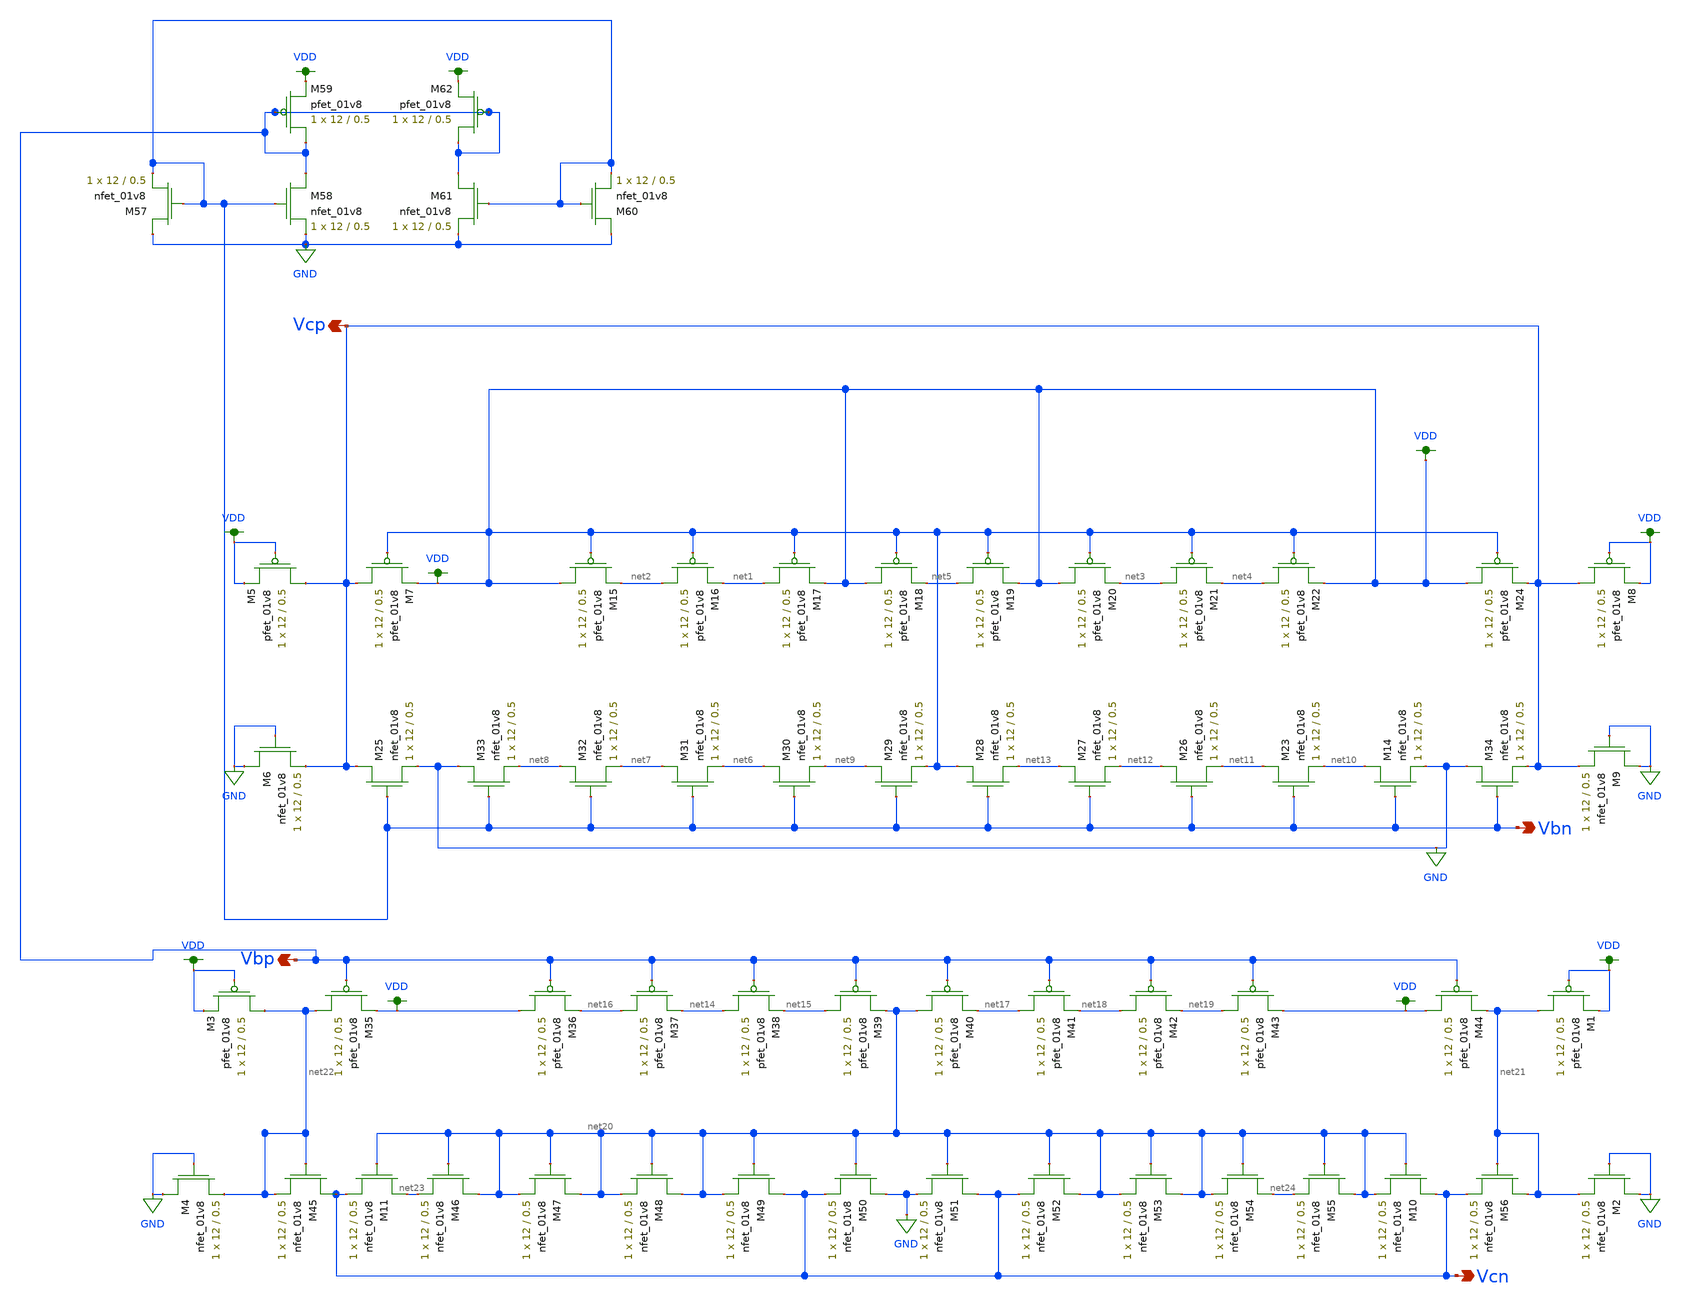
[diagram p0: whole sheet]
** sch_path: miniproject3/LVS_BIASGEN.sch
**.subckt LVS_BIASGEN Vbp Vcn Vcp Vbn
*.opin Vbp
*.opin Vcn
*.opin Vcp
*.opin Vbn
XM7 Vcp VDD VDD VDD sky130_fd_pr__pfet_01v8 L=0.5 W=12 nf=1 ad='int((nf+1)/2) * W/nf * 0.29' as='int((nf+2)/2) * W/nf * 0.29'
+ pd='2*int((nf+1)/2) * (W/nf + 0.29)' ps='2*int((nf+2)/2) * (W/nf + 0.29)' nrd='0.29 / W' nrs='0.29 / W'
+ sa=0 sb=0 sd=0 mult=1 m=1
XM15 VDD VDD net2 VDD sky130_fd_pr__pfet_01v8 L=0.5 W=12 nf=1 ad='int((nf+1)/2) * W/nf * 0.29' as='int((nf+2)/2) * W/nf * 0.29'
+ pd='2*int((nf+1)/2) * (W/nf + 0.29)' ps='2*int((nf+2)/2) * (W/nf + 0.29)' nrd='0.29 / W' nrs='0.29 / W'
+ sa=0 sb=0 sd=0 mult=1 m=1
XM16 net2 VDD net1 VDD sky130_fd_pr__pfet_01v8 L=0.5 W=12 nf=1 ad='int((nf+1)/2) * W/nf * 0.29' as='int((nf+2)/2) * W/nf * 0.29'
+ pd='2*int((nf+1)/2) * (W/nf + 0.29)' ps='2*int((nf+2)/2) * (W/nf + 0.29)' nrd='0.29 / W' nrs='0.29 / W'
+ sa=0 sb=0 sd=0 mult=1 m=1
XM17 net1 VDD VDD VDD sky130_fd_pr__pfet_01v8 L=0.5 W=12 nf=1 ad='int((nf+1)/2) * W/nf * 0.29' as='int((nf+2)/2) * W/nf * 0.29'
+ pd='2*int((nf+1)/2) * (W/nf + 0.29)' ps='2*int((nf+2)/2) * (W/nf + 0.29)' nrd='0.29 / W' nrs='0.29 / W'
+ sa=0 sb=0 sd=0 mult=1 m=1
XM18 VDD VDD net5 VDD sky130_fd_pr__pfet_01v8 L=0.5 W=12 nf=1 ad='int((nf+1)/2) * W/nf * 0.29' as='int((nf+2)/2) * W/nf * 0.29'
+ pd='2*int((nf+1)/2) * (W/nf + 0.29)' ps='2*int((nf+2)/2) * (W/nf + 0.29)' nrd='0.29 / W' nrs='0.29 / W'
+ sa=0 sb=0 sd=0 mult=1 m=1
XM19 net5 VDD VDD VDD sky130_fd_pr__pfet_01v8 L=0.5 W=12 nf=1 ad='int((nf+1)/2) * W/nf * 0.29' as='int((nf+2)/2) * W/nf * 0.29'
+ pd='2*int((nf+1)/2) * (W/nf + 0.29)' ps='2*int((nf+2)/2) * (W/nf + 0.29)' nrd='0.29 / W' nrs='0.29 / W'
+ sa=0 sb=0 sd=0 mult=1 m=1
XM20 VDD VDD net3 VDD sky130_fd_pr__pfet_01v8 L=0.5 W=12 nf=1 ad='int((nf+1)/2) * W/nf * 0.29' as='int((nf+2)/2) * W/nf * 0.29'
+ pd='2*int((nf+1)/2) * (W/nf + 0.29)' ps='2*int((nf+2)/2) * (W/nf + 0.29)' nrd='0.29 / W' nrs='0.29 / W'
+ sa=0 sb=0 sd=0 mult=1 m=1
XM21 net3 VDD net4 VDD sky130_fd_pr__pfet_01v8 L=0.5 W=12 nf=1 ad='int((nf+1)/2) * W/nf * 0.29' as='int((nf+2)/2) * W/nf * 0.29'
+ pd='2*int((nf+1)/2) * (W/nf + 0.29)' ps='2*int((nf+2)/2) * (W/nf + 0.29)' nrd='0.29 / W' nrs='0.29 / W'
+ sa=0 sb=0 sd=0 mult=1 m=1
XM22 net4 VDD VDD VDD sky130_fd_pr__pfet_01v8 L=0.5 W=12 nf=1 ad='int((nf+1)/2) * W/nf * 0.29' as='int((nf+2)/2) * W/nf * 0.29'
+ pd='2*int((nf+1)/2) * (W/nf + 0.29)' ps='2*int((nf+2)/2) * (W/nf + 0.29)' nrd='0.29 / W' nrs='0.29 / W'
+ sa=0 sb=0 sd=0 mult=1 m=1
XM24 VDD VDD Vcp VDD sky130_fd_pr__pfet_01v8 L=0.5 W=12 nf=1 ad='int((nf+1)/2) * W/nf * 0.29' as='int((nf+2)/2) * W/nf * 0.29'
+ pd='2*int((nf+1)/2) * (W/nf + 0.29)' ps='2*int((nf+2)/2) * (W/nf + 0.29)' nrd='0.29 / W' nrs='0.29 / W'
+ sa=0 sb=0 sd=0 mult=1 m=1
XM25 Vcp Vbn GND GND sky130_fd_pr__nfet_01v8 L=0.5 W=12 nf=1 ad='int((nf+1)/2) * W/nf * 0.29' as='int((nf+2)/2) * W/nf * 0.29'
+ pd='2*int((nf+1)/2) * (W/nf + 0.29)' ps='2*int((nf+2)/2) * (W/nf + 0.29)' nrd='0.29 / W' nrs='0.29 / W'
+ sa=0 sb=0 sd=0 mult=1 m=1
XM14 net10 Vbn GND GND sky130_fd_pr__nfet_01v8 L=0.5 W=12 nf=1 ad='int((nf+1)/2) * W/nf * 0.29' as='int((nf+2)/2) * W/nf * 0.29'
+ pd='2*int((nf+1)/2) * (W/nf + 0.29)' ps='2*int((nf+2)/2) * (W/nf + 0.29)' nrd='0.29 / W' nrs='0.29 / W'
+ sa=0 sb=0 sd=0 mult=1 m=1
XM23 net11 Vbn net10 GND sky130_fd_pr__nfet_01v8 L=0.5 W=12 nf=1 ad='int((nf+1)/2) * W/nf * 0.29' as='int((nf+2)/2) * W/nf * 0.29'
+ pd='2*int((nf+1)/2) * (W/nf + 0.29)' ps='2*int((nf+2)/2) * (W/nf + 0.29)' nrd='0.29 / W' nrs='0.29 / W'
+ sa=0 sb=0 sd=0 mult=1 m=1
XM26 net12 Vbn net11 GND sky130_fd_pr__nfet_01v8 L=0.5 W=12 nf=1 ad='int((nf+1)/2) * W/nf * 0.29' as='int((nf+2)/2) * W/nf * 0.29'
+ pd='2*int((nf+1)/2) * (W/nf + 0.29)' ps='2*int((nf+2)/2) * (W/nf + 0.29)' nrd='0.29 / W' nrs='0.29 / W'
+ sa=0 sb=0 sd=0 mult=1 m=1
XM27 net13 Vbn net12 GND sky130_fd_pr__nfet_01v8 L=0.5 W=12 nf=1 ad='int((nf+1)/2) * W/nf * 0.29' as='int((nf+2)/2) * W/nf * 0.29'
+ pd='2*int((nf+1)/2) * (W/nf + 0.29)' ps='2*int((nf+2)/2) * (W/nf + 0.29)' nrd='0.29 / W' nrs='0.29 / W'
+ sa=0 sb=0 sd=0 mult=1 m=1
XM28 VDD Vbn net13 GND sky130_fd_pr__nfet_01v8 L=0.5 W=12 nf=1 ad='int((nf+1)/2) * W/nf * 0.29' as='int((nf+2)/2) * W/nf * 0.29'
+ pd='2*int((nf+1)/2) * (W/nf + 0.29)' ps='2*int((nf+2)/2) * (W/nf + 0.29)' nrd='0.29 / W' nrs='0.29 / W'
+ sa=0 sb=0 sd=0 mult=1 m=1
XM29 net9 Vbn VDD GND sky130_fd_pr__nfet_01v8 L=0.5 W=12 nf=1 ad='int((nf+1)/2) * W/nf * 0.29' as='int((nf+2)/2) * W/nf * 0.29'
+ pd='2*int((nf+1)/2) * (W/nf + 0.29)' ps='2*int((nf+2)/2) * (W/nf + 0.29)' nrd='0.29 / W' nrs='0.29 / W'
+ sa=0 sb=0 sd=0 mult=1 m=1
XM30 net6 Vbn net9 GND sky130_fd_pr__nfet_01v8 L=0.5 W=12 nf=1 ad='int((nf+1)/2) * W/nf * 0.29' as='int((nf+2)/2) * W/nf * 0.29'
+ pd='2*int((nf+1)/2) * (W/nf + 0.29)' ps='2*int((nf+2)/2) * (W/nf + 0.29)' nrd='0.29 / W' nrs='0.29 / W'
+ sa=0 sb=0 sd=0 mult=1 m=1
XM31 net7 Vbn net6 GND sky130_fd_pr__nfet_01v8 L=0.5 W=12 nf=1 ad='int((nf+1)/2) * W/nf * 0.29' as='int((nf+2)/2) * W/nf * 0.29'
+ pd='2*int((nf+1)/2) * (W/nf + 0.29)' ps='2*int((nf+2)/2) * (W/nf + 0.29)' nrd='0.29 / W' nrs='0.29 / W'
+ sa=0 sb=0 sd=0 mult=1 m=1
XM32 net8 Vbn net7 GND sky130_fd_pr__nfet_01v8 L=0.5 W=12 nf=1 ad='int((nf+1)/2) * W/nf * 0.29' as='int((nf+2)/2) * W/nf * 0.29'
+ pd='2*int((nf+1)/2) * (W/nf + 0.29)' ps='2*int((nf+2)/2) * (W/nf + 0.29)' nrd='0.29 / W' nrs='0.29 / W'
+ sa=0 sb=0 sd=0 mult=1 m=1
XM33 GND Vbn net8 GND sky130_fd_pr__nfet_01v8 L=0.5 W=12 nf=1 ad='int((nf+1)/2) * W/nf * 0.29' as='int((nf+2)/2) * W/nf * 0.29'
+ pd='2*int((nf+1)/2) * (W/nf + 0.29)' ps='2*int((nf+2)/2) * (W/nf + 0.29)' nrd='0.29 / W' nrs='0.29 / W'
+ sa=0 sb=0 sd=0 mult=1 m=1
XM34 GND Vbn Vcp GND sky130_fd_pr__nfet_01v8 L=0.5 W=12 nf=1 ad='int((nf+1)/2) * W/nf * 0.29' as='int((nf+2)/2) * W/nf * 0.29'
+ pd='2*int((nf+1)/2) * (W/nf + 0.29)' ps='2*int((nf+2)/2) * (W/nf + 0.29)' nrd='0.29 / W' nrs='0.29 / W'
+ sa=0 sb=0 sd=0 mult=1 m=1
XM35 net22 Vbp VDD VDD sky130_fd_pr__pfet_01v8 L=0.5 W=12 nf=1 ad='int((nf+1)/2) * W/nf * 0.29' as='int((nf+2)/2) * W/nf * 0.29'
+ pd='2*int((nf+1)/2) * (W/nf + 0.29)' ps='2*int((nf+2)/2) * (W/nf + 0.29)' nrd='0.29 / W' nrs='0.29 / W'
+ sa=0 sb=0 sd=0 mult=1 m=1
XM36 VDD Vbp net16 VDD sky130_fd_pr__pfet_01v8 L=0.5 W=12 nf=1 ad='int((nf+1)/2) * W/nf * 0.29' as='int((nf+2)/2) * W/nf * 0.29'
+ pd='2*int((nf+1)/2) * (W/nf + 0.29)' ps='2*int((nf+2)/2) * (W/nf + 0.29)' nrd='0.29 / W' nrs='0.29 / W'
+ sa=0 sb=0 sd=0 mult=1 m=1
XM37 net16 Vbp net14 VDD sky130_fd_pr__pfet_01v8 L=0.5 W=12 nf=1 ad='int((nf+1)/2) * W/nf * 0.29' as='int((nf+2)/2) * W/nf * 0.29'
+ pd='2*int((nf+1)/2) * (W/nf + 0.29)' ps='2*int((nf+2)/2) * (W/nf + 0.29)' nrd='0.29 / W' nrs='0.29 / W'
+ sa=0 sb=0 sd=0 mult=1 m=1
XM38 net14 Vbp net15 VDD sky130_fd_pr__pfet_01v8 L=0.5 W=12 nf=1 ad='int((nf+1)/2) * W/nf * 0.29' as='int((nf+2)/2) * W/nf * 0.29'
+ pd='2*int((nf+1)/2) * (W/nf + 0.29)' ps='2*int((nf+2)/2) * (W/nf + 0.29)' nrd='0.29 / W' nrs='0.29 / W'
+ sa=0 sb=0 sd=0 mult=1 m=1
XM39 net15 Vbp net20 VDD sky130_fd_pr__pfet_01v8 L=0.5 W=12 nf=1 ad='int((nf+1)/2) * W/nf * 0.29' as='int((nf+2)/2) * W/nf * 0.29'
+ pd='2*int((nf+1)/2) * (W/nf + 0.29)' ps='2*int((nf+2)/2) * (W/nf + 0.29)' nrd='0.29 / W' nrs='0.29 / W'
+ sa=0 sb=0 sd=0 mult=1 m=1
XM40 net20 Vbp net17 VDD sky130_fd_pr__pfet_01v8 L=0.5 W=12 nf=1 ad='int((nf+1)/2) * W/nf * 0.29' as='int((nf+2)/2) * W/nf * 0.29'
+ pd='2*int((nf+1)/2) * (W/nf + 0.29)' ps='2*int((nf+2)/2) * (W/nf + 0.29)' nrd='0.29 / W' nrs='0.29 / W'
+ sa=0 sb=0 sd=0 mult=1 m=1
XM41 net17 Vbp net18 VDD sky130_fd_pr__pfet_01v8 L=0.5 W=12 nf=1 ad='int((nf+1)/2) * W/nf * 0.29' as='int((nf+2)/2) * W/nf * 0.29'
+ pd='2*int((nf+1)/2) * (W/nf + 0.29)' ps='2*int((nf+2)/2) * (W/nf + 0.29)' nrd='0.29 / W' nrs='0.29 / W'
+ sa=0 sb=0 sd=0 mult=1 m=1
XM42 net18 Vbp net19 VDD sky130_fd_pr__pfet_01v8 L=0.5 W=12 nf=1 ad='int((nf+1)/2) * W/nf * 0.29' as='int((nf+2)/2) * W/nf * 0.29'
+ pd='2*int((nf+1)/2) * (W/nf + 0.29)' ps='2*int((nf+2)/2) * (W/nf + 0.29)' nrd='0.29 / W' nrs='0.29 / W'
+ sa=0 sb=0 sd=0 mult=1 m=1
XM43 net19 Vbp VDD VDD sky130_fd_pr__pfet_01v8 L=0.5 W=12 nf=1 ad='int((nf+1)/2) * W/nf * 0.29' as='int((nf+2)/2) * W/nf * 0.29'
+ pd='2*int((nf+1)/2) * (W/nf + 0.29)' ps='2*int((nf+2)/2) * (W/nf + 0.29)' nrd='0.29 / W' nrs='0.29 / W'
+ sa=0 sb=0 sd=0 mult=1 m=1
XM44 VDD Vbp net21 VDD sky130_fd_pr__pfet_01v8 L=0.5 W=12 nf=1 ad='int((nf+1)/2) * W/nf * 0.29' as='int((nf+2)/2) * W/nf * 0.29'
+ pd='2*int((nf+1)/2) * (W/nf + 0.29)' ps='2*int((nf+2)/2) * (W/nf + 0.29)' nrd='0.29 / W' nrs='0.29 / W'
+ sa=0 sb=0 sd=0 mult=1 m=1
XM45 Vcn net22 net22 GND sky130_fd_pr__nfet_01v8 L=0.5 W=12 nf=1 ad='int((nf+1)/2) * W/nf * 0.29' as='int((nf+2)/2) * W/nf * 0.29'
+ pd='2*int((nf+1)/2) * (W/nf + 0.29)' ps='2*int((nf+2)/2) * (W/nf + 0.29)' nrd='0.29 / W' nrs='0.29 / W'
+ sa=0 sb=0 sd=0 mult=1 m=1
XM46 net20 net20 net23 GND sky130_fd_pr__nfet_01v8 L=0.5 W=12 nf=1 ad='int((nf+1)/2) * W/nf * 0.29' as='int((nf+2)/2) * W/nf * 0.29'
+ pd='2*int((nf+1)/2) * (W/nf + 0.29)' ps='2*int((nf+2)/2) * (W/nf + 0.29)' nrd='0.29 / W' nrs='0.29 / W'
+ sa=0 sb=0 sd=0 mult=1 m=1
XM47 net20 net20 net20 GND sky130_fd_pr__nfet_01v8 L=0.5 W=12 nf=1 ad='int((nf+1)/2) * W/nf * 0.29' as='int((nf+2)/2) * W/nf * 0.29'
+ pd='2*int((nf+1)/2) * (W/nf + 0.29)' ps='2*int((nf+2)/2) * (W/nf + 0.29)' nrd='0.29 / W' nrs='0.29 / W'
+ sa=0 sb=0 sd=0 mult=1 m=1
XM48 net20 net20 net20 GND sky130_fd_pr__nfet_01v8 L=0.5 W=12 nf=1 ad='int((nf+1)/2) * W/nf * 0.29' as='int((nf+2)/2) * W/nf * 0.29'
+ pd='2*int((nf+1)/2) * (W/nf + 0.29)' ps='2*int((nf+2)/2) * (W/nf + 0.29)' nrd='0.29 / W' nrs='0.29 / W'
+ sa=0 sb=0 sd=0 mult=1 m=1
XM49 Vcn net20 net20 GND sky130_fd_pr__nfet_01v8 L=0.5 W=12 nf=1 ad='int((nf+1)/2) * W/nf * 0.29' as='int((nf+2)/2) * W/nf * 0.29'
+ pd='2*int((nf+1)/2) * (W/nf + 0.29)' ps='2*int((nf+2)/2) * (W/nf + 0.29)' nrd='0.29 / W' nrs='0.29 / W'
+ sa=0 sb=0 sd=0 mult=1 m=1
XM50 GND net20 Vcn GND sky130_fd_pr__nfet_01v8 L=0.5 W=12 nf=1 ad='int((nf+1)/2) * W/nf * 0.29' as='int((nf+2)/2) * W/nf * 0.29'
+ pd='2*int((nf+1)/2) * (W/nf + 0.29)' ps='2*int((nf+2)/2) * (W/nf + 0.29)' nrd='0.29 / W' nrs='0.29 / W'
+ sa=0 sb=0 sd=0 mult=1 m=1
XM51 Vcn net20 GND GND sky130_fd_pr__nfet_01v8 L=0.5 W=12 nf=1 ad='int((nf+1)/2) * W/nf * 0.29' as='int((nf+2)/2) * W/nf * 0.29'
+ pd='2*int((nf+1)/2) * (W/nf + 0.29)' ps='2*int((nf+2)/2) * (W/nf + 0.29)' nrd='0.29 / W' nrs='0.29 / W'
+ sa=0 sb=0 sd=0 mult=1 m=1
XM52 net20 net20 Vcn GND sky130_fd_pr__nfet_01v8 L=0.5 W=12 nf=1 ad='int((nf+1)/2) * W/nf * 0.29' as='int((nf+2)/2) * W/nf * 0.29'
+ pd='2*int((nf+1)/2) * (W/nf + 0.29)' ps='2*int((nf+2)/2) * (W/nf + 0.29)' nrd='0.29 / W' nrs='0.29 / W'
+ sa=0 sb=0 sd=0 mult=1 m=1
XM53 net20 net20 net20 GND sky130_fd_pr__nfet_01v8 L=0.5 W=12 nf=1 ad='int((nf+1)/2) * W/nf * 0.29' as='int((nf+2)/2) * W/nf * 0.29'
+ pd='2*int((nf+1)/2) * (W/nf + 0.29)' ps='2*int((nf+2)/2) * (W/nf + 0.29)' nrd='0.29 / W' nrs='0.29 / W'
+ sa=0 sb=0 sd=0 mult=1 m=1
XM54 net24 net20 net20 GND sky130_fd_pr__nfet_01v8 L=0.5 W=12 nf=1 ad='int((nf+1)/2) * W/nf * 0.29' as='int((nf+2)/2) * W/nf * 0.29'
+ pd='2*int((nf+1)/2) * (W/nf + 0.29)' ps='2*int((nf+2)/2) * (W/nf + 0.29)' nrd='0.29 / W' nrs='0.29 / W'
+ sa=0 sb=0 sd=0 mult=1 m=1
XM55 net20 net20 net24 GND sky130_fd_pr__nfet_01v8 L=0.5 W=12 nf=1 ad='int((nf+1)/2) * W/nf * 0.29' as='int((nf+2)/2) * W/nf * 0.29'
+ pd='2*int((nf+1)/2) * (W/nf + 0.29)' ps='2*int((nf+2)/2) * (W/nf + 0.29)' nrd='0.29 / W' nrs='0.29 / W'
+ sa=0 sb=0 sd=0 mult=1 m=1
XM56 net21 net21 Vcn GND sky130_fd_pr__nfet_01v8 L=0.5 W=12 nf=1 ad='int((nf+1)/2) * W/nf * 0.29' as='int((nf+2)/2) * W/nf * 0.29'
+ pd='2*int((nf+1)/2) * (W/nf + 0.29)' ps='2*int((nf+2)/2) * (W/nf + 0.29)' nrd='0.29 / W' nrs='0.29 / W'
+ sa=0 sb=0 sd=0 mult=1 m=1
XM57 GND Vbn Vbn GND sky130_fd_pr__nfet_01v8 L=0.5 W=12 nf=1 ad='int((nf+1)/2) * W/nf * 0.29' as='int((nf+2)/2) * W/nf * 0.29'
+ pd='2*int((nf+1)/2) * (W/nf + 0.29)' ps='2*int((nf+2)/2) * (W/nf + 0.29)' nrd='0.29 / W' nrs='0.29 / W'
+ sa=0 sb=0 sd=0 mult=1 m=1
XM58 Vbp Vbn GND GND sky130_fd_pr__nfet_01v8 L=0.5 W=12 nf=1 ad='int((nf+1)/2) * W/nf * 0.29' as='int((nf+2)/2) * W/nf * 0.29'
+ pd='2*int((nf+1)/2) * (W/nf + 0.29)' ps='2*int((nf+2)/2) * (W/nf + 0.29)' nrd='0.29 / W' nrs='0.29 / W'
+ sa=0 sb=0 sd=0 mult=1 m=1
XM59 Vbp Vbp VDD VDD sky130_fd_pr__pfet_01v8 L=0.5 W=12 nf=1 ad='int((nf+1)/2) * W/nf * 0.29' as='int((nf+2)/2) * W/nf * 0.29'
+ pd='2*int((nf+1)/2) * (W/nf + 0.29)' ps='2*int((nf+2)/2) * (W/nf + 0.29)' nrd='0.29 / W' nrs='0.29 / W'
+ sa=0 sb=0 sd=0 mult=1 m=1
XM60 GND Vbn Vbn GND sky130_fd_pr__nfet_01v8 L=0.5 W=12 nf=1 ad='int((nf+1)/2) * W/nf * 0.29' as='int((nf+2)/2) * W/nf * 0.29'
+ pd='2*int((nf+1)/2) * (W/nf + 0.29)' ps='2*int((nf+2)/2) * (W/nf + 0.29)' nrd='0.29 / W' nrs='0.29 / W'
+ sa=0 sb=0 sd=0 mult=1 m=1
XM61 Vbp Vbn GND GND sky130_fd_pr__nfet_01v8 L=0.5 W=12 nf=1 ad='int((nf+1)/2) * W/nf * 0.29' as='int((nf+2)/2) * W/nf * 0.29'
+ pd='2*int((nf+1)/2) * (W/nf + 0.29)' ps='2*int((nf+2)/2) * (W/nf + 0.29)' nrd='0.29 / W' nrs='0.29 / W'
+ sa=0 sb=0 sd=0 mult=1 m=1
XM62 Vbp Vbp VDD VDD sky130_fd_pr__pfet_01v8 L=0.5 W=12 nf=1 ad='int((nf+1)/2) * W/nf * 0.29' as='int((nf+2)/2) * W/nf * 0.29'
+ pd='2*int((nf+1)/2) * (W/nf + 0.29)' ps='2*int((nf+2)/2) * (W/nf + 0.29)' nrd='0.29 / W' nrs='0.29 / W'
+ sa=0 sb=0 sd=0 mult=1 m=1
XM1 net21 VDD VDD VDD sky130_fd_pr__pfet_01v8 L=0.5 W=12 nf=1 ad='int((nf+1)/2) * W/nf * 0.29' as='int((nf+2)/2) * W/nf * 0.29'
+ pd='2*int((nf+1)/2) * (W/nf + 0.29)' ps='2*int((nf+2)/2) * (W/nf + 0.29)' nrd='0.29 / W' nrs='0.29 / W'
+ sa=0 sb=0 sd=0 mult=1 m=1
XM2 GND GND net21 GND sky130_fd_pr__nfet_01v8 L=0.5 W=12 nf=1 ad='int((nf+1)/2) * W/nf * 0.29' as='int((nf+2)/2) * W/nf * 0.29'
+ pd='2*int((nf+1)/2) * (W/nf + 0.29)' ps='2*int((nf+2)/2) * (W/nf + 0.29)' nrd='0.29 / W' nrs='0.29 / W'
+ sa=0 sb=0 sd=0 mult=1 m=1
XM3 net22 VDD VDD VDD sky130_fd_pr__pfet_01v8 L=0.5 W=12 nf=1 ad='int((nf+1)/2) * W/nf * 0.29' as='int((nf+2)/2) * W/nf * 0.29'
+ pd='2*int((nf+1)/2) * (W/nf + 0.29)' ps='2*int((nf+2)/2) * (W/nf + 0.29)' nrd='0.29 / W' nrs='0.29 / W'
+ sa=0 sb=0 sd=0 mult=1 m=1
XM4 GND GND net22 GND sky130_fd_pr__nfet_01v8 L=0.5 W=12 nf=1 ad='int((nf+1)/2) * W/nf * 0.29' as='int((nf+2)/2) * W/nf * 0.29'
+ pd='2*int((nf+1)/2) * (W/nf + 0.29)' ps='2*int((nf+2)/2) * (W/nf + 0.29)' nrd='0.29 / W' nrs='0.29 / W'
+ sa=0 sb=0 sd=0 mult=1 m=1
XM5 Vcp VDD VDD VDD sky130_fd_pr__pfet_01v8 L=0.5 W=12 nf=1 ad='int((nf+1)/2) * W/nf * 0.29' as='int((nf+2)/2) * W/nf * 0.29'
+ pd='2*int((nf+1)/2) * (W/nf + 0.29)' ps='2*int((nf+2)/2) * (W/nf + 0.29)' nrd='0.29 / W' nrs='0.29 / W'
+ sa=0 sb=0 sd=0 mult=1 m=1
XM6 GND GND Vcp GND sky130_fd_pr__nfet_01v8 L=0.5 W=12 nf=1 ad='int((nf+1)/2) * W/nf * 0.29' as='int((nf+2)/2) * W/nf * 0.29'
+ pd='2*int((nf+1)/2) * (W/nf + 0.29)' ps='2*int((nf+2)/2) * (W/nf + 0.29)' nrd='0.29 / W' nrs='0.29 / W'
+ sa=0 sb=0 sd=0 mult=1 m=1
XM8 Vcp VDD VDD VDD sky130_fd_pr__pfet_01v8 L=0.5 W=12 nf=1 ad='int((nf+1)/2) * W/nf * 0.29' as='int((nf+2)/2) * W/nf * 0.29'
+ pd='2*int((nf+1)/2) * (W/nf + 0.29)' ps='2*int((nf+2)/2) * (W/nf + 0.29)' nrd='0.29 / W' nrs='0.29 / W'
+ sa=0 sb=0 sd=0 mult=1 m=1
XM9 GND GND Vcp GND sky130_fd_pr__nfet_01v8 L=0.5 W=12 nf=1 ad='int((nf+1)/2) * W/nf * 0.29' as='int((nf+2)/2) * W/nf * 0.29'
+ pd='2*int((nf+1)/2) * (W/nf + 0.29)' ps='2*int((nf+2)/2) * (W/nf + 0.29)' nrd='0.29 / W' nrs='0.29 / W'
+ sa=0 sb=0 sd=0 mult=1 m=1
XM10 Vcn net20 net20 GND sky130_fd_pr__nfet_01v8 L=0.5 W=12 nf=1 ad='int((nf+1)/2) * W/nf * 0.29' as='int((nf+2)/2) * W/nf * 0.29'
+ pd='2*int((nf+1)/2) * (W/nf + 0.29)' ps='2*int((nf+2)/2) * (W/nf + 0.29)' nrd='0.29 / W' nrs='0.29 / W'
+ sa=0 sb=0 sd=0 mult=1 m=1
XM11 net23 net20 Vcn GND sky130_fd_pr__nfet_01v8 L=0.5 W=12 nf=1 ad='int((nf+1)/2) * W/nf * 0.29' as='int((nf+2)/2) * W/nf * 0.29'
+ pd='2*int((nf+1)/2) * (W/nf + 0.29)' ps='2*int((nf+2)/2) * (W/nf + 0.29)' nrd='0.29 / W' nrs='0.29 / W'
+ sa=0 sb=0 sd=0 mult=1 m=1
**.ends
.GLOBAL VDD
.GLOBAL GND
.end
